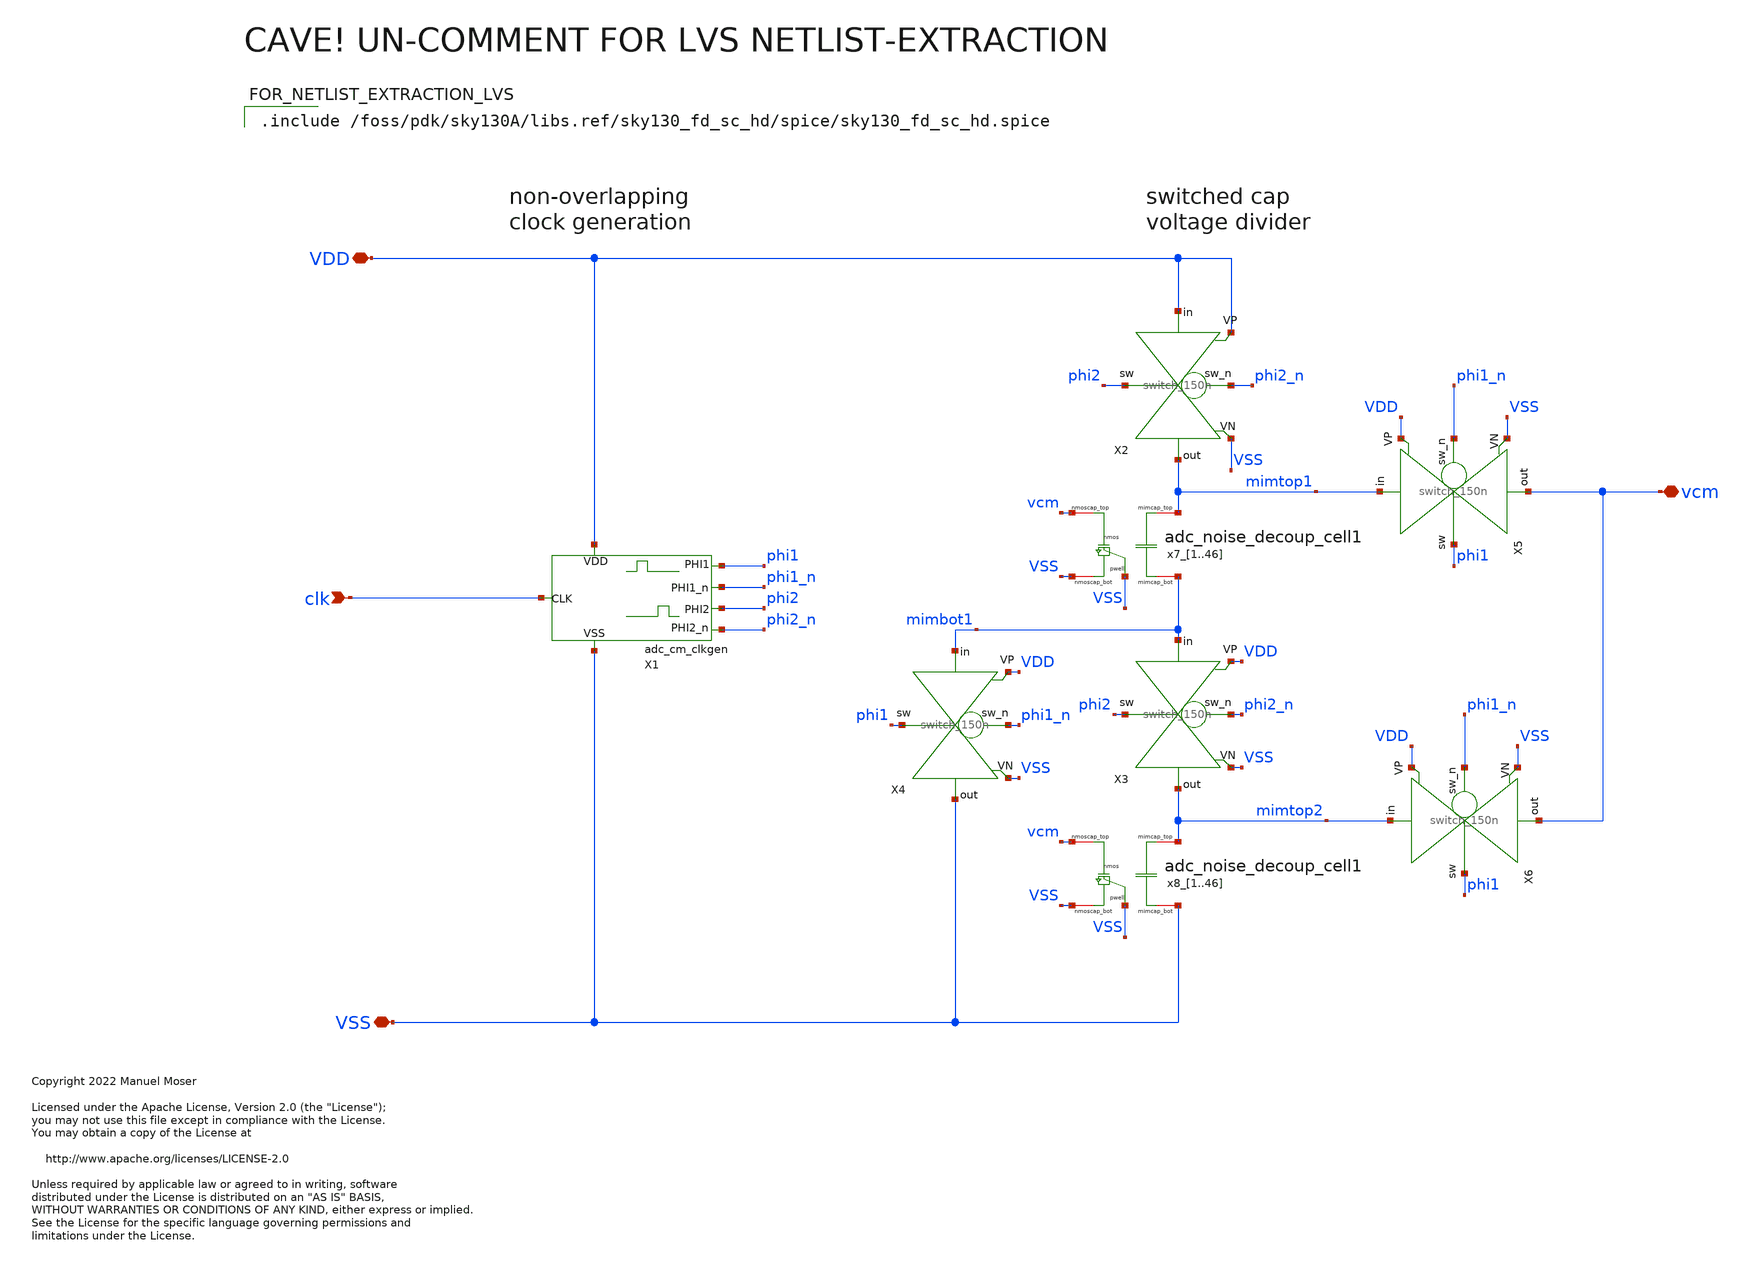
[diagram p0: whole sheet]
** sch_path: xschem/adc_vcm_gen/adc_vcm_gen.sch
* Copyright 2022 Manuel Moser
* Licensed under the Apache License, Version 2.0 (the "License");
**.subckt adc_vcm_gen VDD VSS clk vcm
*.iopin VDD
*.iopin VSS
*.ipin clk
*.iopin vcm
X1 clk VDD VSS phi1_n phi1 phi2 phi2_n adc_cm_clkgen
X2 phi2_n VDD phi2 mimtop1 VDD VSS switch_150n
X3 phi2_n mimbot1 phi2 mimtop2 VDD VSS switch_150n
X4 phi1_n mimbot1 phi1 VSS VDD VSS switch_150n
X5 phi1_n mimtop1 phi1 vcm VDD VSS switch_150n
X6 phi1_n mimtop2 phi1 vcm VDD VSS switch_150n
x7_1 mimtop1 mimbot1 vcm VSS VSS adc_noise_decoup_cell1
x7_2 mimtop1 mimbot1 vcm VSS VSS adc_noise_decoup_cell1
x7_3 mimtop1 mimbot1 vcm VSS VSS adc_noise_decoup_cell1
x7_4 mimtop1 mimbot1 vcm VSS VSS adc_noise_decoup_cell1
x7_5 mimtop1 mimbot1 vcm VSS VSS adc_noise_decoup_cell1
x7_6 mimtop1 mimbot1 vcm VSS VSS adc_noise_decoup_cell1
x7_7 mimtop1 mimbot1 vcm VSS VSS adc_noise_decoup_cell1
x7_8 mimtop1 mimbot1 vcm VSS VSS adc_noise_decoup_cell1
x7_9 mimtop1 mimbot1 vcm VSS VSS adc_noise_decoup_cell1
x7_10 mimtop1 mimbot1 vcm VSS VSS adc_noise_decoup_cell1
x7_11 mimtop1 mimbot1 vcm VSS VSS adc_noise_decoup_cell1
x7_12 mimtop1 mimbot1 vcm VSS VSS adc_noise_decoup_cell1
x7_13 mimtop1 mimbot1 vcm VSS VSS adc_noise_decoup_cell1
x7_14 mimtop1 mimbot1 vcm VSS VSS adc_noise_decoup_cell1
x7_15 mimtop1 mimbot1 vcm VSS VSS adc_noise_decoup_cell1
x7_16 mimtop1 mimbot1 vcm VSS VSS adc_noise_decoup_cell1
x7_17 mimtop1 mimbot1 vcm VSS VSS adc_noise_decoup_cell1
x7_18 mimtop1 mimbot1 vcm VSS VSS adc_noise_decoup_cell1
x7_19 mimtop1 mimbot1 vcm VSS VSS adc_noise_decoup_cell1
x7_20 mimtop1 mimbot1 vcm VSS VSS adc_noise_decoup_cell1
x7_21 mimtop1 mimbot1 vcm VSS VSS adc_noise_decoup_cell1
x7_22 mimtop1 mimbot1 vcm VSS VSS adc_noise_decoup_cell1
x7_23 mimtop1 mimbot1 vcm VSS VSS adc_noise_decoup_cell1
x7_24 mimtop1 mimbot1 vcm VSS VSS adc_noise_decoup_cell1
x7_25 mimtop1 mimbot1 vcm VSS VSS adc_noise_decoup_cell1
x7_26 mimtop1 mimbot1 vcm VSS VSS adc_noise_decoup_cell1
x7_27 mimtop1 mimbot1 vcm VSS VSS adc_noise_decoup_cell1
x7_28 mimtop1 mimbot1 vcm VSS VSS adc_noise_decoup_cell1
x7_29 mimtop1 mimbot1 vcm VSS VSS adc_noise_decoup_cell1
x7_30 mimtop1 mimbot1 vcm VSS VSS adc_noise_decoup_cell1
x7_31 mimtop1 mimbot1 vcm VSS VSS adc_noise_decoup_cell1
x7_32 mimtop1 mimbot1 vcm VSS VSS adc_noise_decoup_cell1
x7_33 mimtop1 mimbot1 vcm VSS VSS adc_noise_decoup_cell1
x7_34 mimtop1 mimbot1 vcm VSS VSS adc_noise_decoup_cell1
x7_35 mimtop1 mimbot1 vcm VSS VSS adc_noise_decoup_cell1
x7_36 mimtop1 mimbot1 vcm VSS VSS adc_noise_decoup_cell1
x7_37 mimtop1 mimbot1 vcm VSS VSS adc_noise_decoup_cell1
x7_38 mimtop1 mimbot1 vcm VSS VSS adc_noise_decoup_cell1
x7_39 mimtop1 mimbot1 vcm VSS VSS adc_noise_decoup_cell1
x7_40 mimtop1 mimbot1 vcm VSS VSS adc_noise_decoup_cell1
x7_41 mimtop1 mimbot1 vcm VSS VSS adc_noise_decoup_cell1
x7_42 mimtop1 mimbot1 vcm VSS VSS adc_noise_decoup_cell1
x7_43 mimtop1 mimbot1 vcm VSS VSS adc_noise_decoup_cell1
x7_44 mimtop1 mimbot1 vcm VSS VSS adc_noise_decoup_cell1
x7_45 mimtop1 mimbot1 vcm VSS VSS adc_noise_decoup_cell1
x7_46 mimtop1 mimbot1 vcm VSS VSS adc_noise_decoup_cell1
x8_1 mimtop2 VSS vcm VSS VSS adc_noise_decoup_cell1
x8_2 mimtop2 VSS vcm VSS VSS adc_noise_decoup_cell1
x8_3 mimtop2 VSS vcm VSS VSS adc_noise_decoup_cell1
x8_4 mimtop2 VSS vcm VSS VSS adc_noise_decoup_cell1
x8_5 mimtop2 VSS vcm VSS VSS adc_noise_decoup_cell1
x8_6 mimtop2 VSS vcm VSS VSS adc_noise_decoup_cell1
x8_7 mimtop2 VSS vcm VSS VSS adc_noise_decoup_cell1
x8_8 mimtop2 VSS vcm VSS VSS adc_noise_decoup_cell1
x8_9 mimtop2 VSS vcm VSS VSS adc_noise_decoup_cell1
x8_10 mimtop2 VSS vcm VSS VSS adc_noise_decoup_cell1
x8_11 mimtop2 VSS vcm VSS VSS adc_noise_decoup_cell1
x8_12 mimtop2 VSS vcm VSS VSS adc_noise_decoup_cell1
x8_13 mimtop2 VSS vcm VSS VSS adc_noise_decoup_cell1
x8_14 mimtop2 VSS vcm VSS VSS adc_noise_decoup_cell1
x8_15 mimtop2 VSS vcm VSS VSS adc_noise_decoup_cell1
x8_16 mimtop2 VSS vcm VSS VSS adc_noise_decoup_cell1
x8_17 mimtop2 VSS vcm VSS VSS adc_noise_decoup_cell1
x8_18 mimtop2 VSS vcm VSS VSS adc_noise_decoup_cell1
x8_19 mimtop2 VSS vcm VSS VSS adc_noise_decoup_cell1
x8_20 mimtop2 VSS vcm VSS VSS adc_noise_decoup_cell1
x8_21 mimtop2 VSS vcm VSS VSS adc_noise_decoup_cell1
x8_22 mimtop2 VSS vcm VSS VSS adc_noise_decoup_cell1
x8_23 mimtop2 VSS vcm VSS VSS adc_noise_decoup_cell1
x8_24 mimtop2 VSS vcm VSS VSS adc_noise_decoup_cell1
x8_25 mimtop2 VSS vcm VSS VSS adc_noise_decoup_cell1
x8_26 mimtop2 VSS vcm VSS VSS adc_noise_decoup_cell1
x8_27 mimtop2 VSS vcm VSS VSS adc_noise_decoup_cell1
x8_28 mimtop2 VSS vcm VSS VSS adc_noise_decoup_cell1
x8_29 mimtop2 VSS vcm VSS VSS adc_noise_decoup_cell1
x8_30 mimtop2 VSS vcm VSS VSS adc_noise_decoup_cell1
x8_31 mimtop2 VSS vcm VSS VSS adc_noise_decoup_cell1
x8_32 mimtop2 VSS vcm VSS VSS adc_noise_decoup_cell1
x8_33 mimtop2 VSS vcm VSS VSS adc_noise_decoup_cell1
x8_34 mimtop2 VSS vcm VSS VSS adc_noise_decoup_cell1
x8_35 mimtop2 VSS vcm VSS VSS adc_noise_decoup_cell1
x8_36 mimtop2 VSS vcm VSS VSS adc_noise_decoup_cell1
x8_37 mimtop2 VSS vcm VSS VSS adc_noise_decoup_cell1
x8_38 mimtop2 VSS vcm VSS VSS adc_noise_decoup_cell1
x8_39 mimtop2 VSS vcm VSS VSS adc_noise_decoup_cell1
x8_40 mimtop2 VSS vcm VSS VSS adc_noise_decoup_cell1
x8_41 mimtop2 VSS vcm VSS VSS adc_noise_decoup_cell1
x8_42 mimtop2 VSS vcm VSS VSS adc_noise_decoup_cell1
x8_43 mimtop2 VSS vcm VSS VSS adc_noise_decoup_cell1
x8_44 mimtop2 VSS vcm VSS VSS adc_noise_decoup_cell1
x8_45 mimtop2 VSS vcm VSS VSS adc_noise_decoup_cell1
x8_46 mimtop2 VSS vcm VSS VSS adc_noise_decoup_cell1
**** begin user architecture code

.include /foss/pdk/sky130A/libs.ref/sky130_fd_sc_hd/spice/sky130_fd_sc_hd.spice

**** end user architecture code
**.ends
.end
